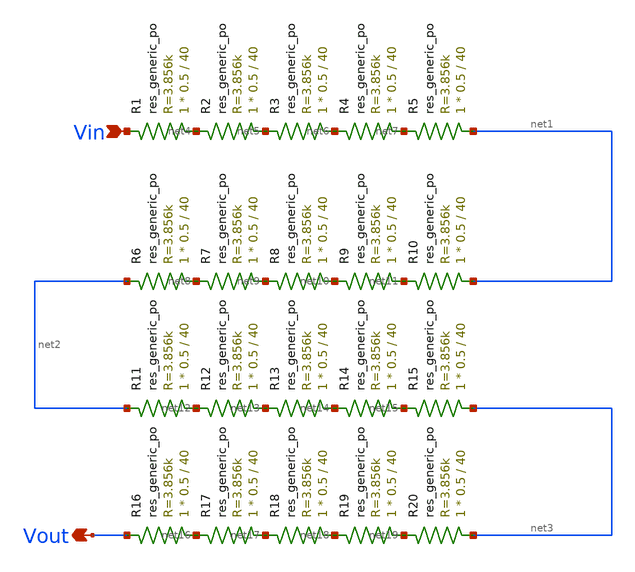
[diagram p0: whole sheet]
** sch_path: src/Opamp_Design/src/res_pack.sch
**.subckt res_pack Vin Vout
*.ipin Vin
*.opin Vout
XR1 net4 Vin sky130_fd_pr__res_generic_po W=0.5 L=40 m=1
XR2 net5 net4 sky130_fd_pr__res_generic_po W=0.5 L=40 m=1
XR3 net6 net5 sky130_fd_pr__res_generic_po W=0.5 L=40 m=1
XR4 net7 net6 sky130_fd_pr__res_generic_po W=0.5 L=40 m=1
XR5 net1 net7 sky130_fd_pr__res_generic_po W=0.5 L=40 m=1
XR6 net8 net2 sky130_fd_pr__res_generic_po W=0.5 L=40 m=1
XR7 net9 net8 sky130_fd_pr__res_generic_po W=0.5 L=40 m=1
XR8 net10 net9 sky130_fd_pr__res_generic_po W=0.5 L=40 m=1
XR9 net11 net10 sky130_fd_pr__res_generic_po W=0.5 L=40 m=1
XR10 net1 net11 sky130_fd_pr__res_generic_po W=0.5 L=40 m=1
XR11 net12 net2 sky130_fd_pr__res_generic_po W=0.5 L=40 m=1
XR12 net13 net12 sky130_fd_pr__res_generic_po W=0.5 L=40 m=1
XR13 net14 net13 sky130_fd_pr__res_generic_po W=0.5 L=40 m=1
XR14 net15 net14 sky130_fd_pr__res_generic_po W=0.5 L=40 m=1
XR16 net16 Vout sky130_fd_pr__res_generic_po W=0.5 L=40 m=1
XR17 net17 net16 sky130_fd_pr__res_generic_po W=0.5 L=40 m=1
XR18 net18 net17 sky130_fd_pr__res_generic_po W=0.5 L=40 m=1
XR19 net19 net18 sky130_fd_pr__res_generic_po W=0.5 L=40 m=1
XR20 net3 net19 sky130_fd_pr__res_generic_po W=0.5 L=40 m=1
XR15 net3 net15 sky130_fd_pr__res_generic_po W=0.5 L=40 m=1
**.ends
.end
